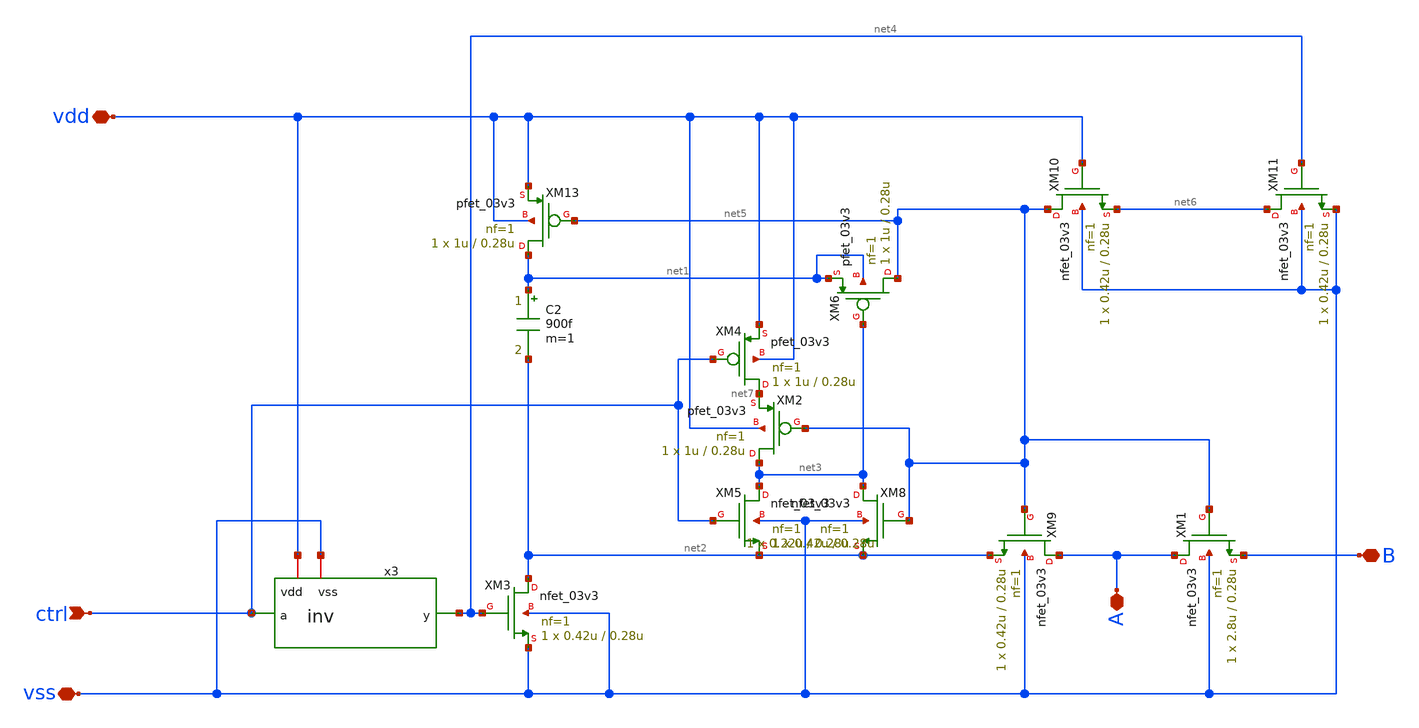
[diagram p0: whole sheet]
** sch_path: member_project/ice458/dynamic_comparator/xschem/bt_sw.sch
**.subckt bt_sw ctrl A B vdd vss
*.ipin ctrl
*.iopin A
*.iopin B
*.iopin vdd
*.iopin vss
XM1 A net5 B vss nfet_03v3 L=0.28u W=2.8u nf=1 ad='int((nf+1)/2) * W/nf * 0.18u' as='int((nf+2)/2) * W/nf * 0.18u'
+ pd='2*int((nf+1)/2) * (W/nf + 0.18u)' ps='2*int((nf+2)/2) * (W/nf + 0.18u)' nrd='0.18u / W' nrs='0.18u / W'
+ sa=0 sb=0 sd=0 m=1
C2 net1 net2 900f m=1
XM8 net3 net5 net2 vss nfet_03v3 L=0.28u W=0.22u nf=1 ad='int((nf+1)/2) * W/nf * 0.18u' as='int((nf+2)/2) * W/nf * 0.18u'
+ pd='2*int((nf+1)/2) * (W/nf + 0.18u)' ps='2*int((nf+2)/2) * (W/nf + 0.18u)' nrd='0.18u / W' nrs='0.18u / W'
+ sa=0 sb=0 sd=0 m=1
x3 vdd ctrl net4 vss inv
XM13 net1 net5 vdd vdd pfet_03v3 L=0.28u W=1u nf=1 ad='int((nf+1)/2) * W/nf * 0.18u' as='int((nf+2)/2) * W/nf * 0.18u'
+ pd='2*int((nf+1)/2) * (W/nf + 0.18u)' ps='2*int((nf+2)/2) * (W/nf + 0.18u)' nrd='0.18u / W' nrs='0.18u / W'
+ sa=0 sb=0 sd=0 m=1
XM3 net2 net4 vss vss nfet_03v3 L=0.28u W=0.42u nf=1 ad='int((nf+1)/2) * W/nf * 0.18u' as='int((nf+2)/2) * W/nf * 0.18u'
+ pd='2*int((nf+1)/2) * (W/nf + 0.18u)' ps='2*int((nf+2)/2) * (W/nf + 0.18u)' nrd='0.18u / W' nrs='0.18u / W'
+ sa=0 sb=0 sd=0 m=1
XM5 net3 ctrl net2 vss nfet_03v3 L=0.28u W=0.42u nf=1 ad='int((nf+1)/2) * W/nf * 0.18u' as='int((nf+2)/2) * W/nf * 0.18u'
+ pd='2*int((nf+1)/2) * (W/nf + 0.18u)' ps='2*int((nf+2)/2) * (W/nf + 0.18u)' nrd='0.18u / W' nrs='0.18u / W'
+ sa=0 sb=0 sd=0 m=1
XM9 A net5 net2 vss nfet_03v3 L=0.28u W=0.42u nf=1 ad='int((nf+1)/2) * W/nf * 0.18u' as='int((nf+2)/2) * W/nf * 0.18u'
+ pd='2*int((nf+1)/2) * (W/nf + 0.18u)' ps='2*int((nf+2)/2) * (W/nf + 0.18u)' nrd='0.18u / W' nrs='0.18u / W'
+ sa=0 sb=0 sd=0 m=1
XM10 net5 vdd net6 vss nfet_03v3 L=0.28u W=0.42u nf=1 ad='int((nf+1)/2) * W/nf * 0.18u' as='int((nf+2)/2) * W/nf * 0.18u'
+ pd='2*int((nf+1)/2) * (W/nf + 0.18u)' ps='2*int((nf+2)/2) * (W/nf + 0.18u)' nrd='0.18u / W' nrs='0.18u / W'
+ sa=0 sb=0 sd=0 m=1
XM11 net6 net4 vss vss nfet_03v3 L=0.28u W=0.42u nf=1 ad='int((nf+1)/2) * W/nf * 0.18u' as='int((nf+2)/2) * W/nf * 0.18u'
+ pd='2*int((nf+1)/2) * (W/nf + 0.18u)' ps='2*int((nf+2)/2) * (W/nf + 0.18u)' nrd='0.18u / W' nrs='0.18u / W'
+ sa=0 sb=0 sd=0 m=1
XM2 net3 net5 net7 vdd pfet_03v3 L=0.28u W=1u nf=1 ad='int((nf+1)/2) * W/nf * 0.18u' as='int((nf+2)/2) * W/nf * 0.18u'
+ pd='2*int((nf+1)/2) * (W/nf + 0.18u)' ps='2*int((nf+2)/2) * (W/nf + 0.18u)' nrd='0.18u / W' nrs='0.18u / W'
+ sa=0 sb=0 sd=0 m=1
XM4 net7 ctrl vdd vdd pfet_03v3 L=0.28u W=1u nf=1 ad='int((nf+1)/2) * W/nf * 0.18u' as='int((nf+2)/2) * W/nf * 0.18u'
+ pd='2*int((nf+1)/2) * (W/nf + 0.18u)' ps='2*int((nf+2)/2) * (W/nf + 0.18u)' nrd='0.18u / W' nrs='0.18u / W'
+ sa=0 sb=0 sd=0 m=1
XM6 net5 net3 net1 net1 pfet_03v3 L=0.28u W=1u nf=1 ad='int((nf+1)/2) * W/nf * 0.18u' as='int((nf+2)/2) * W/nf * 0.18u'
+ pd='2*int((nf+1)/2) * (W/nf + 0.18u)' ps='2*int((nf+2)/2) * (W/nf + 0.18u)' nrd='0.18u / W' nrs='0.18u / W'
+ sa=0 sb=0 sd=0 m=1
**.ends

* expanding   symbol:  inv.sym # of pins=4
** sym_path: member_project/ice458/dynamic_comparator/xschem/inv.sym
** sch_path: member_project/ice458/dynamic_comparator/xschem/inv.sch
.subckt inv vdd a y vss
*.iopin vdd
*.iopin vss
*.ipin a
*.opin y
XM1 y a vss vss nfet_03v3 L=0.28u W=0.42u nf=1 ad='int((nf+1)/2) * W/nf * 0.18u' as='int((nf+2)/2) * W/nf * 0.18u'
+ pd='2*int((nf+1)/2) * (W/nf + 0.18u)' ps='2*int((nf+2)/2) * (W/nf + 0.18u)' nrd='0.18u / W' nrs='0.18u / W'
+ sa=0 sb=0 sd=0 m=1
XM2 y a vdd vdd pfet_03v3 L=0.28u W=1u nf=1 ad='int((nf+1)/2) * W/nf * 0.18u' as='int((nf+2)/2) * W/nf * 0.18u'
+ pd='2*int((nf+1)/2) * (W/nf + 0.18u)' ps='2*int((nf+2)/2) * (W/nf + 0.18u)' nrd='0.18u / W' nrs='0.18u / W'
+ sa=0 sb=0 sd=0 m=1
.ends

.end
